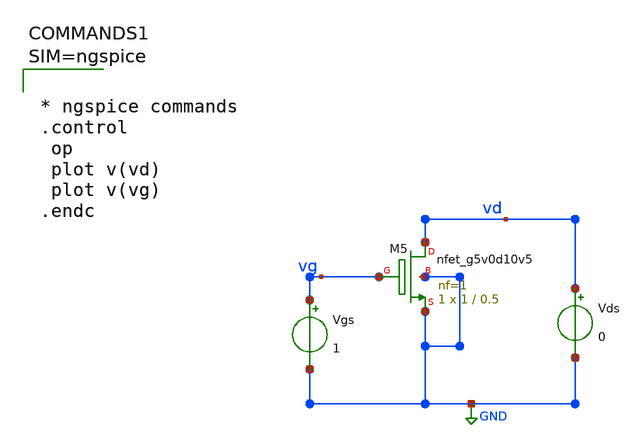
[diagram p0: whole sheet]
** sch_path: xschem/nfet_M5.sch
**.subckt nfet_M5
Vgs vg GND 1
Vds vd GND 0
XM5 vd vg GND GND sky130_fd_pr__nfet_g5v0d10v5 L=0.5 W=1 nf=1 ad='int((1 + 1)/2) * 1 / 1 * 0.29' as='int((1 + 2)/2) * 1 / 1 * 0.29'
+ pd='2*int((1 + 1)/2) * (1 / 1 + 0.29)' ps='2*int((1 + 2)/2) * (1 / 1 + 0.29)' nrd='0.29 / 1 ' nrs='0.29 / 1 '
+ sa=0 sb=0 sd=0 mult=1 m=1
**** begin user architecture code

** opencircuitdesign pdks install
.lib $::SKYWATER_MODELS/sky130.lib.spice tt




* ngspice commands
.control
 op
 plot v(vd)
 plot v(vg)
.endc




** opencircuitdesign pdks install
.lib $::SKYWATER_MODELS/sky130.lib.spice tt




* ngspice commands
.control
 op
 plot v(vd)
 plot v(vg)
.endc



**** end user architecture code
**.ends
.GLOBAL GND
.end
